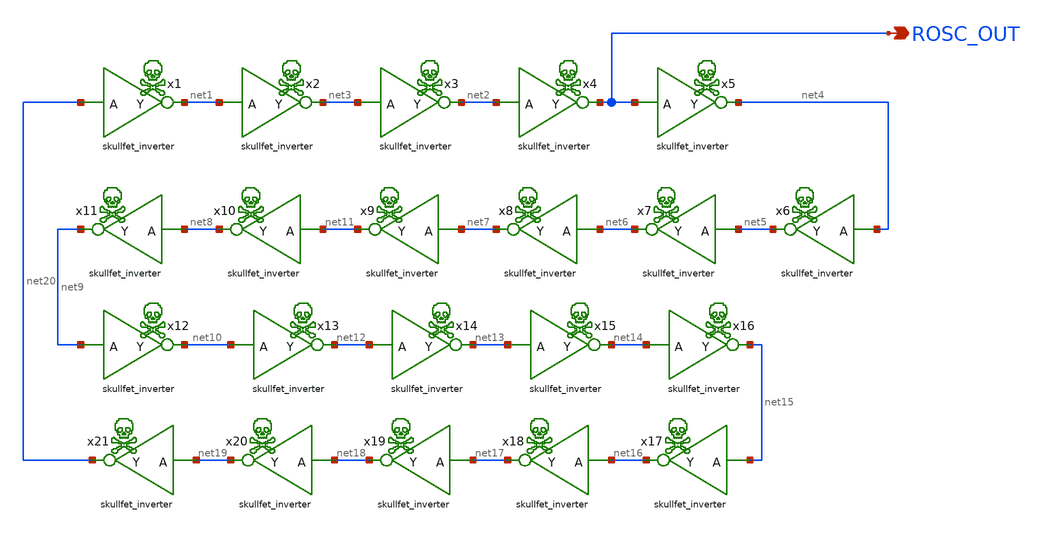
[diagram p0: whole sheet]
** sch_path: xschem/ring.sch
**.subckt ring ROSC_OUT
*.opin ROSC_OUT
x1 net20 net1 skullfet_inverter
x2 net1 net3 skullfet_inverter
x3 net3 net2 skullfet_inverter
x4 net2 ROSC_OUT skullfet_inverter
x5 ROSC_OUT net4 skullfet_inverter
x7 net5 net6 skullfet_inverter
x6 net4 net5 skullfet_inverter
x8 net6 net7 skullfet_inverter
x9 net7 net11 skullfet_inverter
x10 net11 net8 skullfet_inverter
x11 net8 net9 skullfet_inverter
x12 net9 net10 skullfet_inverter
x13 net10 net12 skullfet_inverter
x14 net12 net13 skullfet_inverter
x15 net13 net14 skullfet_inverter
x16 net14 net15 skullfet_inverter
x17 net15 net16 skullfet_inverter
x18 net16 net17 skullfet_inverter
x19 net17 net18 skullfet_inverter
x20 net18 net19 skullfet_inverter
x21 net19 net20 skullfet_inverter
**** begin user architecture code


* Set an initial condition on net1 (0.0001 V) to break symmetry and assist DC operating point
*+ convergence in ngspice
.ic V(net1)=0.0001


**** end user architecture code
**.ends

* expanding   symbol:  skullfet_inverter.sym # of pins=2
** sym_path: xschem/skullfet_inverter.sym
** sch_path: xschem/skullfet_inverter.sch
.subckt skullfet_inverter A Y
*.ipin A
*.opin Y
XM1 Y A VDPWR VDPWR sg13_lv_pmos w=0.15u l=0.13u ng=1 m=1 mm_ok=1
XM2 Y A VGND VGND sg13_lv_nmos w=0.15u l=0.13u ng=1 m=1 mm_ok=1
.ends

.GLOBAL VGND
.GLOBAL VDPWR
.end
